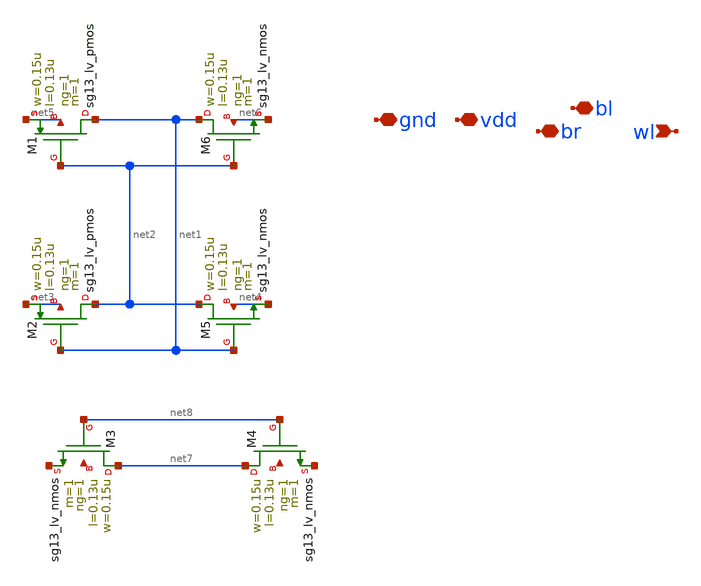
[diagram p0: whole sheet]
** sch_path: xschem/cell_1rw.sch
**.subckt cell_1rw gnd vdd bl br wl
*.iopin gnd
*.iopin vdd
*.iopin bl
*.iopin br
*.ipin wl
XM1 net1 net2 net5 net5 sg13_lv_pmos w=0.15u l=0.13u ng=1 m=1 mm_ok=1
XM2 net2 net1 net3 net3 sg13_lv_pmos w=0.15u l=0.13u ng=1 m=1 mm_ok=1
XM3 net7 net8 net9 net10 sg13_lv_nmos w=0.15u l=0.13u ng=1 m=1 mm_ok=1
XM4 net7 net8 net11 net12 sg13_lv_nmos w=0.15u l=0.13u ng=1 m=1 mm_ok=1
XM5 net2 net1 net4 net4 sg13_lv_nmos w=0.15u l=0.13u ng=1 m=1 mm_ok=1
XM6 net1 net2 net6 net6 sg13_lv_nmos w=0.15u l=0.13u ng=1 m=1 mm_ok=1
**.ends
.end
